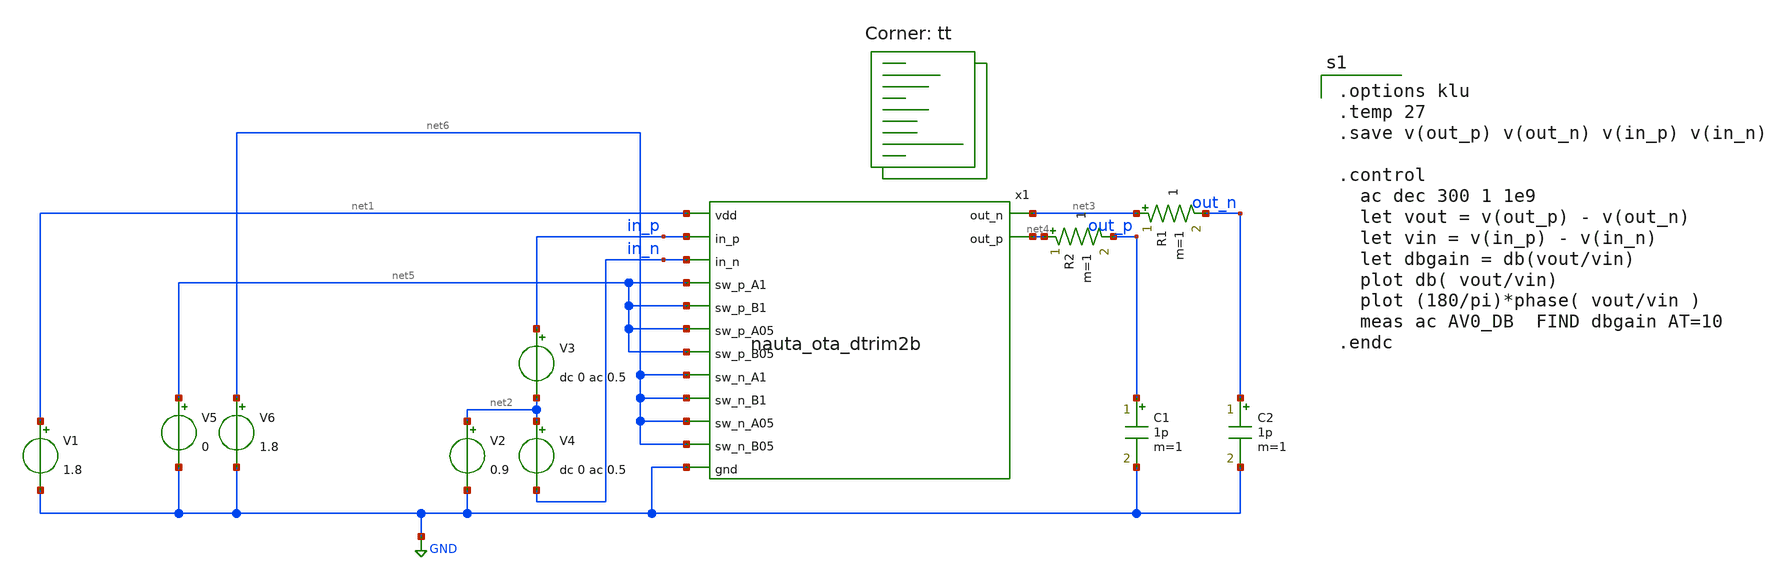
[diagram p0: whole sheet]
** sch_path: xsch/nauta_ota_dtrim2b_tb.sch
**.subckt nauta_ota_dtrim2b_tb
V1 net1 GND 1.8
V2 net2 GND 0.9
V3 in_p net2 dc 0 ac 0.5
V4 net2 in_n dc 0 ac 0.5
C1 out_p GND 1p m=1
C2 out_n GND 1p m=1
V5 net5 GND 0
V6 net6 GND 1.8
x1 net1 net3 in_p net4 in_n net5 net5 net5 net5 net6 net6 net6 net6 GND nauta_ota_dtrim2b
R1 net3 out_n 1 m=1
R2 net4 out_p 1 m=1
**** begin user architecture code
.lib $::SKYWATER_MODELS/sky130.lib.spice tt

.options klu
.temp 27
.save v(out_p) v(out_n) v(in_p) v(in_n)

.control
  ac dec 300 1 1e9
  let vout = v(out_p) - v(out_n)
  let vin = v(in_p) - v(in_n)
  let dbgain = db(vout/vin)
  plot db( vout/vin)
  plot (180/pi)*phase( vout/vin )
  meas ac AV0_DB  FIND dbgain AT=10
.endc



**** end user architecture code
**.ends
.GLOBAL GND
.end
